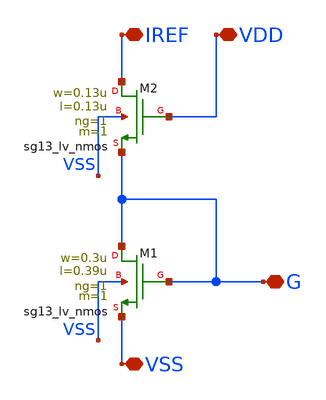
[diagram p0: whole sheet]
** sch_path: W2W-DAC/W2W_BOX/current_nmos.sch
**.subckt current_nmos VSS IREF VDD G
*.iopin VSS
*.iopin IREF
*.iopin VDD
*.iopin G
XM2 IREF VDD G VSS sg13_lv_nmos w=0.13u l=0.13u ng=1 m=1 mm_ok=1
XM1 G G VSS VSS sg13_lv_nmos w=0.3u l=0.39u ng=1 m=1 mm_ok=1
**.ends
.end
